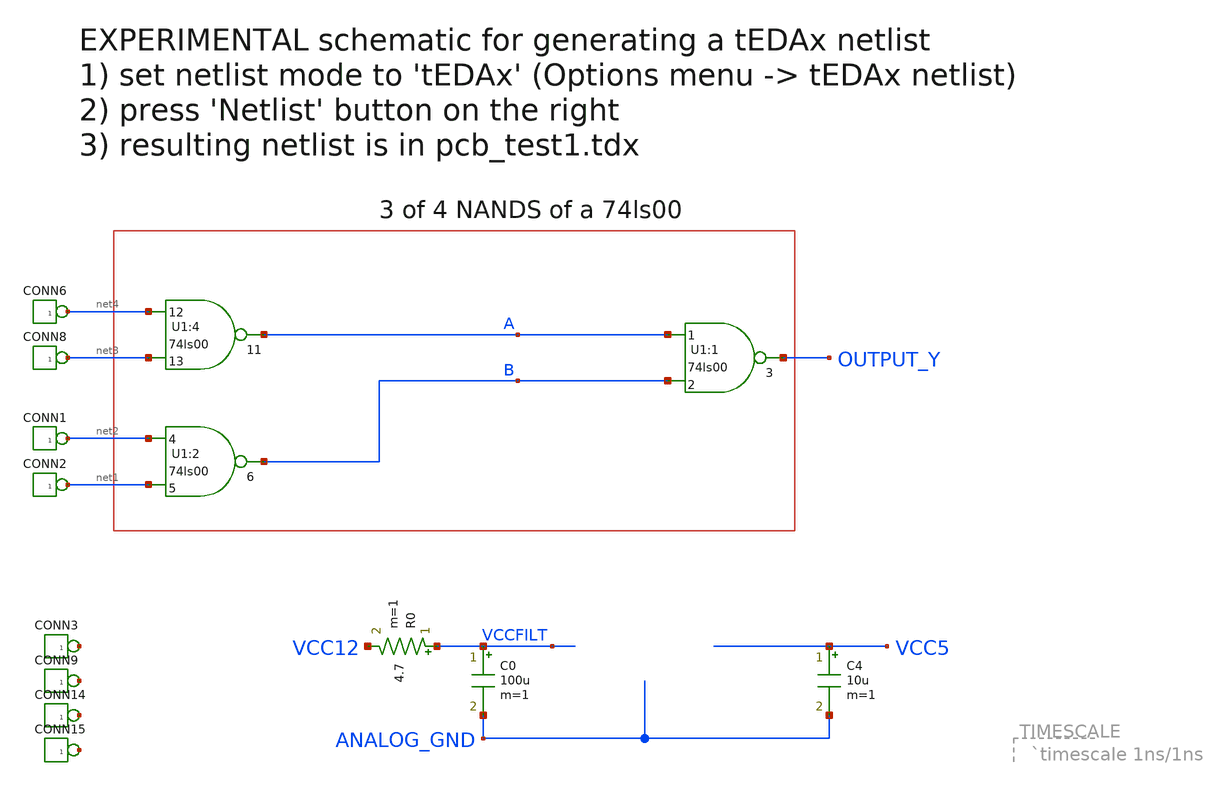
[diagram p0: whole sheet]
** sch_path: assets/pcb_test1.sch
**.subckt pcb_test1
U1:2 net2 net1 B
U1:1 A B OUTPUT_Y
C0 VCCFILT ANALOG_GND 100u m=1
U1:4 net4 net3 A
C4 VCC5 ANALOG_GND 10u m=1
R0 VCCFILT VCC12 4.7 m=1
*connector(1,1) ?1 net2
*connector(1,1) ?1 net1
*connector(1,1) ?1 net5
*connector(1,1) ?1 net4
*connector(1,1) ?1 net3
*connector(1,1) ?1 net6
*connector(1,1) ?1 net7
*connector(1,1) ?1 net8
**** begin user architecture code

initial begin
  $dumpfile("dumpfile.vcd");
  $dumpvars;
  INPUT_E=0;
  INPUT_F=0;
  INPUT_A=0;
  INPUT_B=0;
  ANALOG_GND=0;
  #10000;
  INPUT_A=1;
  INPUT_B=1;
  #10000;
  INPUT_E=1;
  INPUT_F=1;
  #10000;
  INPUT_F=0;
  #10000;
  INPUT_B=0;
  #10000;
  $finish;
end

assign VCC12=1;



**** end user architecture code
**.ends
.end
